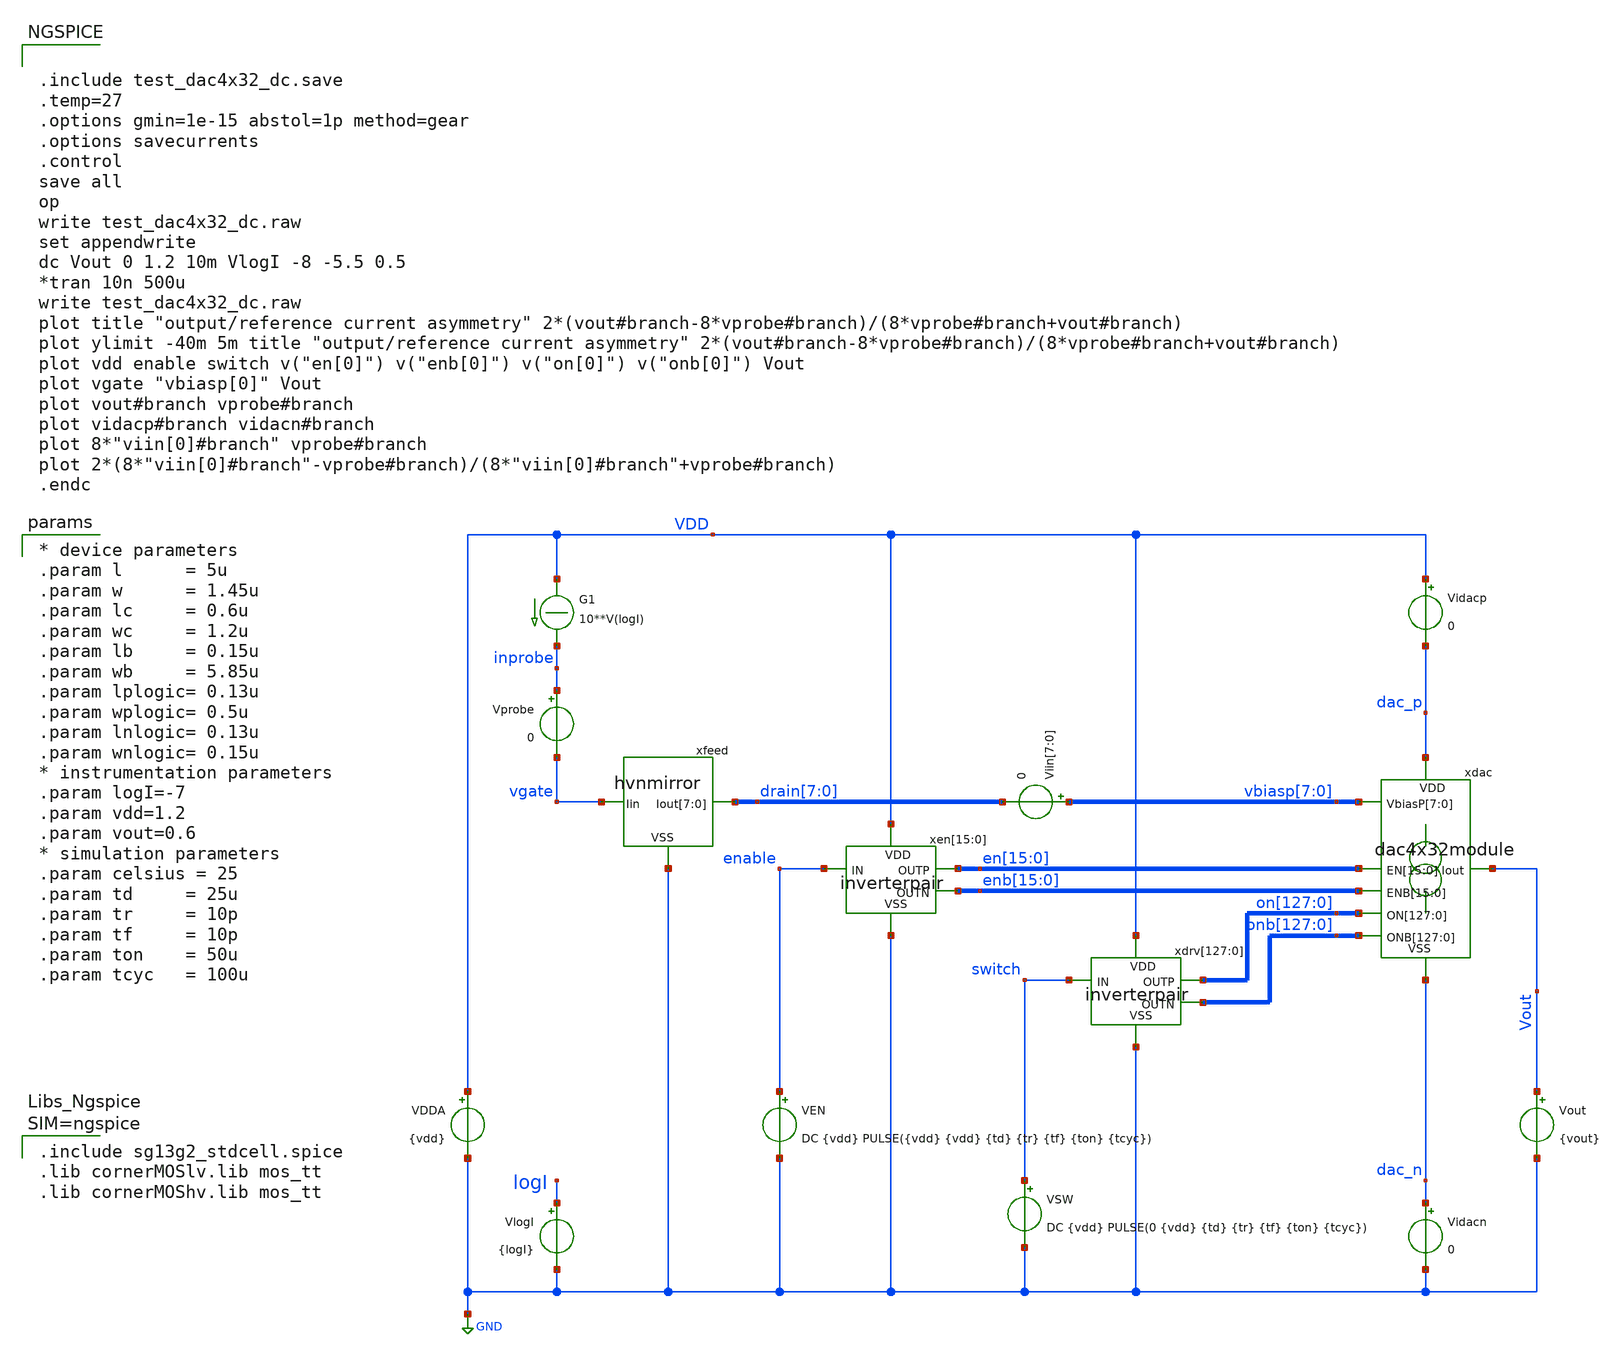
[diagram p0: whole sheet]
** sch_path: xschem/test_dac4x32_dc.sch
**.subckt test_dac4x32_dc
Vout Vout GND {vout}
.save i(vout)
Vprobe inprobe vgate 0
.save i(vprobe)
G1 VDD inprobe CUR=' 10**V(logI) '
VlogI logI GND {logI}
.save i(vlogi)
VDDA VDD GND {vdd}
.save i(vdda)
VSW switch GND DC {vdd} PULSE(0 {vdd} {td} {tr} {tf} {ton} {tcyc})
.save i(vsw)
Vidacp VDD dac_p 0
.save i(vidacp)
Vidacn dac_n GND 0
.save i(vidacn)
xdac dac_p en[15] en[14] en[13] en[12] en[11] en[10] en[9] en[8] en[7] en[6] en[5] en[4] en[3] en[2]
+ en[1] en[0] enb[15] enb[14] enb[13] enb[12] enb[11] enb[10] enb[9] enb[8] enb[7] enb[6] enb[5] enb[4]
+ enb[3] enb[2] enb[1] enb[0] on[127] on[126] on[125] on[124] on[123] on[122] on[121] on[120] on[119]
+ on[118] on[117] on[116] on[115] on[114] on[113] on[112] on[111] on[110] on[109] on[108] on[107] on[106]
+ on[105] on[104] on[103] on[102] on[101] on[100] on[99] on[98] on[97] on[96] on[95] on[94] on[93] on[92]
+ on[91] on[90] on[89] on[88] on[87] on[86] on[85] on[84] on[83] on[82] on[81] on[80] on[79] on[78] on[77]
+ on[76] on[75] on[74] on[73] on[72] on[71] on[70] on[69] on[68] on[67] on[66] on[65] on[64] on[63] on[62]
+ on[61] on[60] on[59] on[58] on[57] on[56] on[55] on[54] on[53] on[52] on[51] on[50] on[49] on[48] on[47]
+ on[46] on[45] on[44] on[43] on[42] on[41] on[40] on[39] on[38] on[37] on[36] on[35] on[34] on[33] on[32]
+ on[31] on[30] on[29] on[28] on[27] on[26] on[25] on[24] on[23] on[22] on[21] on[20] on[19] on[18] on[17]
+ on[16] on[15] on[14] on[13] on[12] on[11] on[10] on[9] on[8] on[7] on[6] on[5] on[4] on[3] on[2] on[1]
+ on[0] onb[127] onb[126] onb[125] onb[124] onb[123] onb[122] onb[121] onb[120] onb[119] onb[118] onb[117]
+ onb[116] onb[115] onb[114] onb[113] onb[112] onb[111] onb[110] onb[109] onb[108] onb[107] onb[106] onb[105]
+ onb[104] onb[103] onb[102] onb[101] onb[100] onb[99] onb[98] onb[97] onb[96] onb[95] onb[94] onb[93] onb[92]
+ onb[91] onb[90] onb[89] onb[88] onb[87] onb[86] onb[85] onb[84] onb[83] onb[82] onb[81] onb[80] onb[79]
+ onb[78] onb[77] onb[76] onb[75] onb[74] onb[73] onb[72] onb[71] onb[70] onb[69] onb[68] onb[67] onb[66]
+ onb[65] onb[64] onb[63] onb[62] onb[61] onb[60] onb[59] onb[58] onb[57] onb[56] onb[55] onb[54] onb[53]
+ onb[52] onb[51] onb[50] onb[49] onb[48] onb[47] onb[46] onb[45] onb[44] onb[43] onb[42] onb[41] onb[40]
+ onb[39] onb[38] onb[37] onb[36] onb[35] onb[34] onb[33] onb[32] onb[31] onb[30] onb[29] onb[28] onb[27]
+ onb[26] onb[25] onb[24] onb[23] onb[22] onb[21] onb[20] onb[19] onb[18] onb[17] onb[16] onb[15] onb[14]
+ onb[13] onb[12] onb[11] onb[10] onb[9] onb[8] onb[7] onb[6] onb[5] onb[4] onb[3] onb[2] onb[1] onb[0] Vout
+ vbiasp[7] vbiasp[6] vbiasp[5] vbiasp[4] vbiasp[3] vbiasp[2] vbiasp[1] vbiasp[0] dac_n dac4x32module
xen[15] VDD en[15] enable enb[15] GND inverterpair
xen[14] VDD en[14] enable enb[14] GND inverterpair
xen[13] VDD en[13] enable enb[13] GND inverterpair
xen[12] VDD en[12] enable enb[12] GND inverterpair
xen[11] VDD en[11] enable enb[11] GND inverterpair
xen[10] VDD en[10] enable enb[10] GND inverterpair
xen[9] VDD en[9] enable enb[9] GND inverterpair
xen[8] VDD en[8] enable enb[8] GND inverterpair
xen[7] VDD en[7] enable enb[7] GND inverterpair
xen[6] VDD en[6] enable enb[6] GND inverterpair
xen[5] VDD en[5] enable enb[5] GND inverterpair
xen[4] VDD en[4] enable enb[4] GND inverterpair
xen[3] VDD en[3] enable enb[3] GND inverterpair
xen[2] VDD en[2] enable enb[2] GND inverterpair
xen[1] VDD en[1] enable enb[1] GND inverterpair
xen[0] VDD en[0] enable enb[0] GND inverterpair
xdrv[127] VDD on[127] switch onb[127] GND inverterpair
xdrv[126] VDD on[126] switch onb[126] GND inverterpair
xdrv[125] VDD on[125] switch onb[125] GND inverterpair
xdrv[124] VDD on[124] switch onb[124] GND inverterpair
xdrv[123] VDD on[123] switch onb[123] GND inverterpair
xdrv[122] VDD on[122] switch onb[122] GND inverterpair
xdrv[121] VDD on[121] switch onb[121] GND inverterpair
xdrv[120] VDD on[120] switch onb[120] GND inverterpair
xdrv[119] VDD on[119] switch onb[119] GND inverterpair
xdrv[118] VDD on[118] switch onb[118] GND inverterpair
xdrv[117] VDD on[117] switch onb[117] GND inverterpair
xdrv[116] VDD on[116] switch onb[116] GND inverterpair
xdrv[115] VDD on[115] switch onb[115] GND inverterpair
xdrv[114] VDD on[114] switch onb[114] GND inverterpair
xdrv[113] VDD on[113] switch onb[113] GND inverterpair
xdrv[112] VDD on[112] switch onb[112] GND inverterpair
xdrv[111] VDD on[111] switch onb[111] GND inverterpair
xdrv[110] VDD on[110] switch onb[110] GND inverterpair
xdrv[109] VDD on[109] switch onb[109] GND inverterpair
xdrv[108] VDD on[108] switch onb[108] GND inverterpair
xdrv[107] VDD on[107] switch onb[107] GND inverterpair
xdrv[106] VDD on[106] switch onb[106] GND inverterpair
xdrv[105] VDD on[105] switch onb[105] GND inverterpair
xdrv[104] VDD on[104] switch onb[104] GND inverterpair
xdrv[103] VDD on[103] switch onb[103] GND inverterpair
xdrv[102] VDD on[102] switch onb[102] GND inverterpair
xdrv[101] VDD on[101] switch onb[101] GND inverterpair
xdrv[100] VDD on[100] switch onb[100] GND inverterpair
xdrv[99] VDD on[99] switch onb[99] GND inverterpair
xdrv[98] VDD on[98] switch onb[98] GND inverterpair
xdrv[97] VDD on[97] switch onb[97] GND inverterpair
xdrv[96] VDD on[96] switch onb[96] GND inverterpair
xdrv[95] VDD on[95] switch onb[95] GND inverterpair
xdrv[94] VDD on[94] switch onb[94] GND inverterpair
xdrv[93] VDD on[93] switch onb[93] GND inverterpair
xdrv[92] VDD on[92] switch onb[92] GND inverterpair
xdrv[91] VDD on[91] switch onb[91] GND inverterpair
xdrv[90] VDD on[90] switch onb[90] GND inverterpair
xdrv[89] VDD on[89] switch onb[89] GND inverterpair
xdrv[88] VDD on[88] switch onb[88] GND inverterpair
xdrv[87] VDD on[87] switch onb[87] GND inverterpair
xdrv[86] VDD on[86] switch onb[86] GND inverterpair
xdrv[85] VDD on[85] switch onb[85] GND inverterpair
xdrv[84] VDD on[84] switch onb[84] GND inverterpair
xdrv[83] VDD on[83] switch onb[83] GND inverterpair
xdrv[82] VDD on[82] switch onb[82] GND inverterpair
xdrv[81] VDD on[81] switch onb[81] GND inverterpair
xdrv[80] VDD on[80] switch onb[80] GND inverterpair
xdrv[79] VDD on[79] switch onb[79] GND inverterpair
xdrv[78] VDD on[78] switch onb[78] GND inverterpair
xdrv[77] VDD on[77] switch onb[77] GND inverterpair
xdrv[76] VDD on[76] switch onb[76] GND inverterpair
xdrv[75] VDD on[75] switch onb[75] GND inverterpair
xdrv[74] VDD on[74] switch onb[74] GND inverterpair
xdrv[73] VDD on[73] switch onb[73] GND inverterpair
xdrv[72] VDD on[72] switch onb[72] GND inverterpair
xdrv[71] VDD on[71] switch onb[71] GND inverterpair
xdrv[70] VDD on[70] switch onb[70] GND inverterpair
xdrv[69] VDD on[69] switch onb[69] GND inverterpair
xdrv[68] VDD on[68] switch onb[68] GND inverterpair
xdrv[67] VDD on[67] switch onb[67] GND inverterpair
xdrv[66] VDD on[66] switch onb[66] GND inverterpair
xdrv[65] VDD on[65] switch onb[65] GND inverterpair
xdrv[64] VDD on[64] switch onb[64] GND inverterpair
xdrv[63] VDD on[63] switch onb[63] GND inverterpair
xdrv[62] VDD on[62] switch onb[62] GND inverterpair
xdrv[61] VDD on[61] switch onb[61] GND inverterpair
xdrv[60] VDD on[60] switch onb[60] GND inverterpair
xdrv[59] VDD on[59] switch onb[59] GND inverterpair
xdrv[58] VDD on[58] switch onb[58] GND inverterpair
xdrv[57] VDD on[57] switch onb[57] GND inverterpair
xdrv[56] VDD on[56] switch onb[56] GND inverterpair
xdrv[55] VDD on[55] switch onb[55] GND inverterpair
xdrv[54] VDD on[54] switch onb[54] GND inverterpair
xdrv[53] VDD on[53] switch onb[53] GND inverterpair
xdrv[52] VDD on[52] switch onb[52] GND inverterpair
xdrv[51] VDD on[51] switch onb[51] GND inverterpair
xdrv[50] VDD on[50] switch onb[50] GND inverterpair
xdrv[49] VDD on[49] switch onb[49] GND inverterpair
xdrv[48] VDD on[48] switch onb[48] GND inverterpair
xdrv[47] VDD on[47] switch onb[47] GND inverterpair
xdrv[46] VDD on[46] switch onb[46] GND inverterpair
xdrv[45] VDD on[45] switch onb[45] GND inverterpair
xdrv[44] VDD on[44] switch onb[44] GND inverterpair
xdrv[43] VDD on[43] switch onb[43] GND inverterpair
xdrv[42] VDD on[42] switch onb[42] GND inverterpair
xdrv[41] VDD on[41] switch onb[41] GND inverterpair
xdrv[40] VDD on[40] switch onb[40] GND inverterpair
xdrv[39] VDD on[39] switch onb[39] GND inverterpair
xdrv[38] VDD on[38] switch onb[38] GND inverterpair
xdrv[37] VDD on[37] switch onb[37] GND inverterpair
xdrv[36] VDD on[36] switch onb[36] GND inverterpair
xdrv[35] VDD on[35] switch onb[35] GND inverterpair
xdrv[34] VDD on[34] switch onb[34] GND inverterpair
xdrv[33] VDD on[33] switch onb[33] GND inverterpair
xdrv[32] VDD on[32] switch onb[32] GND inverterpair
xdrv[31] VDD on[31] switch onb[31] GND inverterpair
xdrv[30] VDD on[30] switch onb[30] GND inverterpair
xdrv[29] VDD on[29] switch onb[29] GND inverterpair
xdrv[28] VDD on[28] switch onb[28] GND inverterpair
xdrv[27] VDD on[27] switch onb[27] GND inverterpair
xdrv[26] VDD on[26] switch onb[26] GND inverterpair
xdrv[25] VDD on[25] switch onb[25] GND inverterpair
xdrv[24] VDD on[24] switch onb[24] GND inverterpair
xdrv[23] VDD on[23] switch onb[23] GND inverterpair
xdrv[22] VDD on[22] switch onb[22] GND inverterpair
xdrv[21] VDD on[21] switch onb[21] GND inverterpair
xdrv[20] VDD on[20] switch onb[20] GND inverterpair
xdrv[19] VDD on[19] switch onb[19] GND inverterpair
xdrv[18] VDD on[18] switch onb[18] GND inverterpair
xdrv[17] VDD on[17] switch onb[17] GND inverterpair
xdrv[16] VDD on[16] switch onb[16] GND inverterpair
xdrv[15] VDD on[15] switch onb[15] GND inverterpair
xdrv[14] VDD on[14] switch onb[14] GND inverterpair
xdrv[13] VDD on[13] switch onb[13] GND inverterpair
xdrv[12] VDD on[12] switch onb[12] GND inverterpair
xdrv[11] VDD on[11] switch onb[11] GND inverterpair
xdrv[10] VDD on[10] switch onb[10] GND inverterpair
xdrv[9] VDD on[9] switch onb[9] GND inverterpair
xdrv[8] VDD on[8] switch onb[8] GND inverterpair
xdrv[7] VDD on[7] switch onb[7] GND inverterpair
xdrv[6] VDD on[6] switch onb[6] GND inverterpair
xdrv[5] VDD on[5] switch onb[5] GND inverterpair
xdrv[4] VDD on[4] switch onb[4] GND inverterpair
xdrv[3] VDD on[3] switch onb[3] GND inverterpair
xdrv[2] VDD on[2] switch onb[2] GND inverterpair
xdrv[1] VDD on[1] switch onb[1] GND inverterpair
xdrv[0] VDD on[0] switch onb[0] GND inverterpair
VEN enable GND DC {vdd} PULSE({vdd} {vdd} {td} {tr} {tf} {ton} {tcyc})
.save i(ven)
xfeed vgate drain[7] drain[6] drain[5] drain[4] drain[3] drain[2] drain[1] drain[0] GND hvnmirror
Viin[7] vbiasp[7] drain[7] 0
Viin[6] vbiasp[6] drain[6] 0
Viin[5] vbiasp[5] drain[5] 0
Viin[4] vbiasp[4] drain[4] 0
Viin[3] vbiasp[3] drain[3] 0
Viin[2] vbiasp[2] drain[2] 0
Viin[1] vbiasp[1] drain[1] 0
Viin[0] vbiasp[0] drain[0] 0
.save i(viin[7])
.save i(viin[6])
.save i(viin[5])
.save i(viin[4])
.save i(viin[3])
.save i(viin[2])
.save i(viin[1])
.save i(viin[0])
**** begin user architecture code


.include test_dac4x32_dc.save
.temp=27
.options gmin=1e-15 abstol=1p method=gear
.options savecurrents
.control
save all
op
write test_dac4x32_dc.raw
set appendwrite
dc Vout 0 1.2 10m VlogI -8 -5.5 0.5
*tran 10n 500u
write test_dac4x32_dc.raw
plot title "output/reference current asymmetry"
+ 2*(vout#branch-8*vprobe#branch)/(8*vprobe#branch+vout#branch)
plot ylimit -40m 5m title "output/reference current asymmetry"
+ 2*(vout#branch-8*vprobe#branch)/(8*vprobe#branch+vout#branch)
plot vdd enable switch v("en[0]") v("enb[0]") v("on[0]") v("onb[0]") Vout
plot vgate "vbiasp[0]" Vout
plot vout#branch vprobe#branch
plot vidacp#branch vidacn#branch
plot 8*"viin[0]#branch" vprobe#branch
plot 2*(8*"viin[0]#branch"-vprobe#branch)/(8*"viin[0]#branch"+vprobe#branch)
.endc




.include sg13g2_stdcell.spice
.lib cornerMOSlv.lib mos_tt
.lib cornerMOShv.lib mos_tt



* device parameters
.param l      = 5u
.param w      = 1.45u
.param lc     = 0.6u
.param wc     = 1.2u
.param lb     = 0.15u
.param wb     = 5.85u
.param lplogic= 0.13u
.param wplogic= 0.5u
.param lnlogic= 0.13u
.param wnlogic= 0.15u
* instrumentation parameters
.param logI=-7
.param vdd=1.2
.param vout=0.6
* simulation parameters
.param celsius = 25
.param td     = 25u
.param tr     = 10p
.param tf     = 10p
.param ton    = 50u
.param tcyc   = 100u


**** end user architecture code
**.ends
.GLOBAL GND
.end
